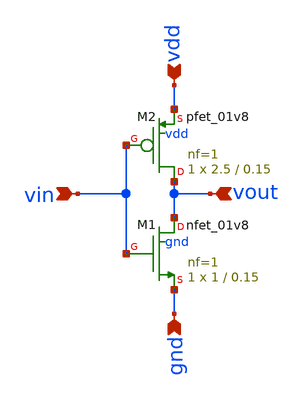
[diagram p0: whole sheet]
** sch_path: working_dir/inv_vtc.sch
**.subckt inv_vtc vin vout gnd vdd
*.ipin vin
*.ipin vout
*.ipin gnd
*.ipin vdd
XM1 vout vin gnd gnd sky130_fd_pr__nfet_01v8 L=0.15 W=1 nf=1 ad='int((nf+1)/2) * W/nf * 0.29' as='int((nf+2)/2) * W/nf * 0.29'
+ pd='2*int((nf+1)/2) * (W/nf + 0.29)' ps='2*int((nf+2)/2) * (W/nf + 0.29)' nrd='0.29 / W' nrs='0.29 / W'
+ sa=0 sb=0 sd=0 mult=1 m=1
XM2 vout vin vdd vdd sky130_fd_pr__pfet_01v8 L=0.15 W=2.5 nf=1 ad='int((nf+1)/2) * W/nf * 0.29' as='int((nf+2)/2) * W/nf * 0.29'
+ pd='2*int((nf+1)/2) * (W/nf + 0.29)' ps='2*int((nf+2)/2) * (W/nf + 0.29)' nrd='0.29 / W' nrs='0.29 / W'
+ sa=0 sb=0 sd=0 mult=1 m=1
**.ends
.end
